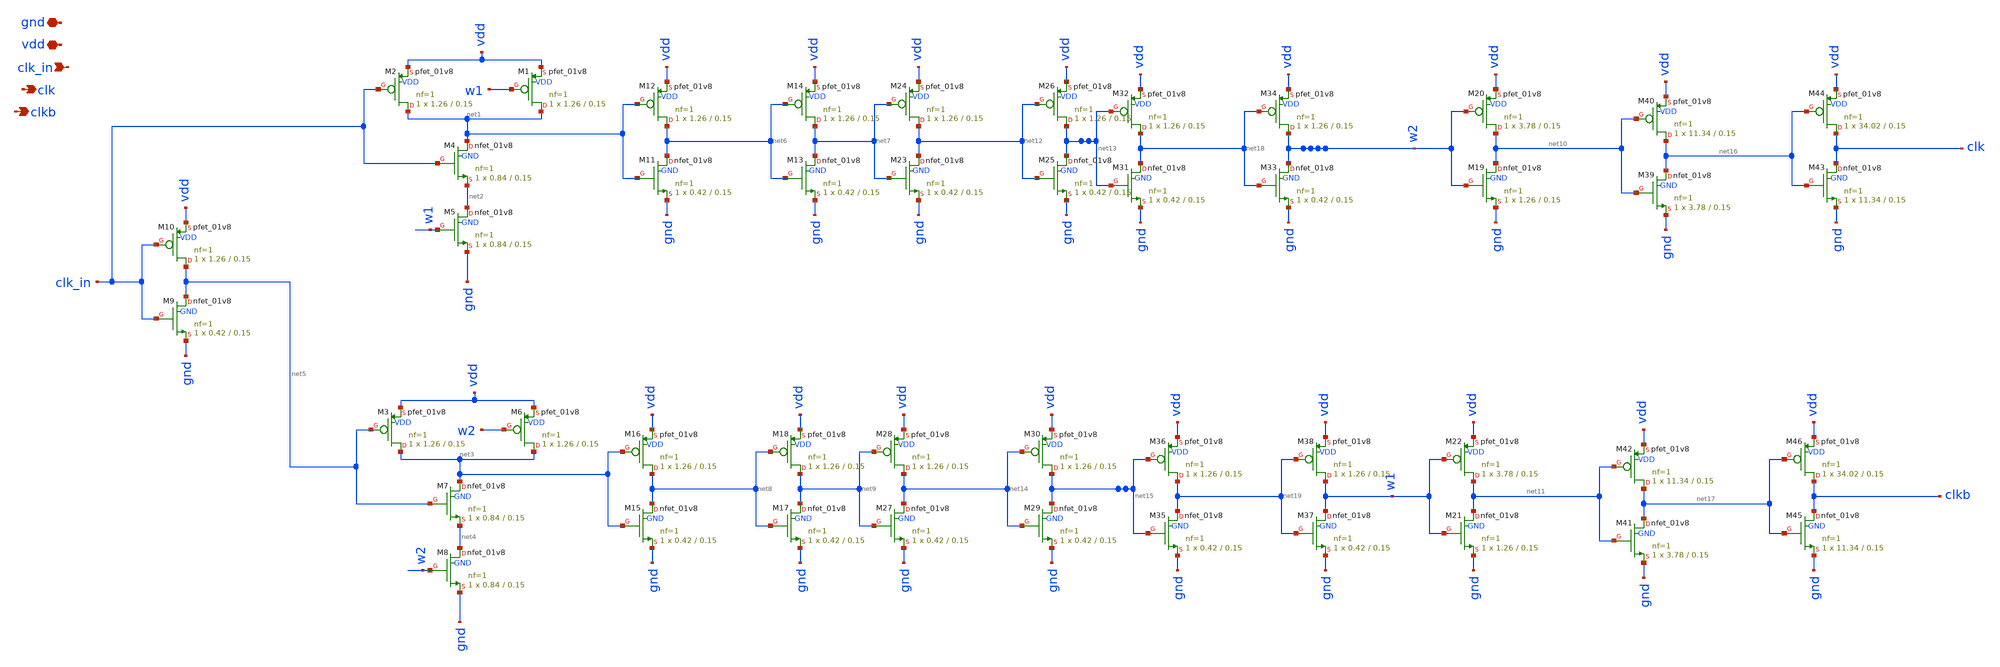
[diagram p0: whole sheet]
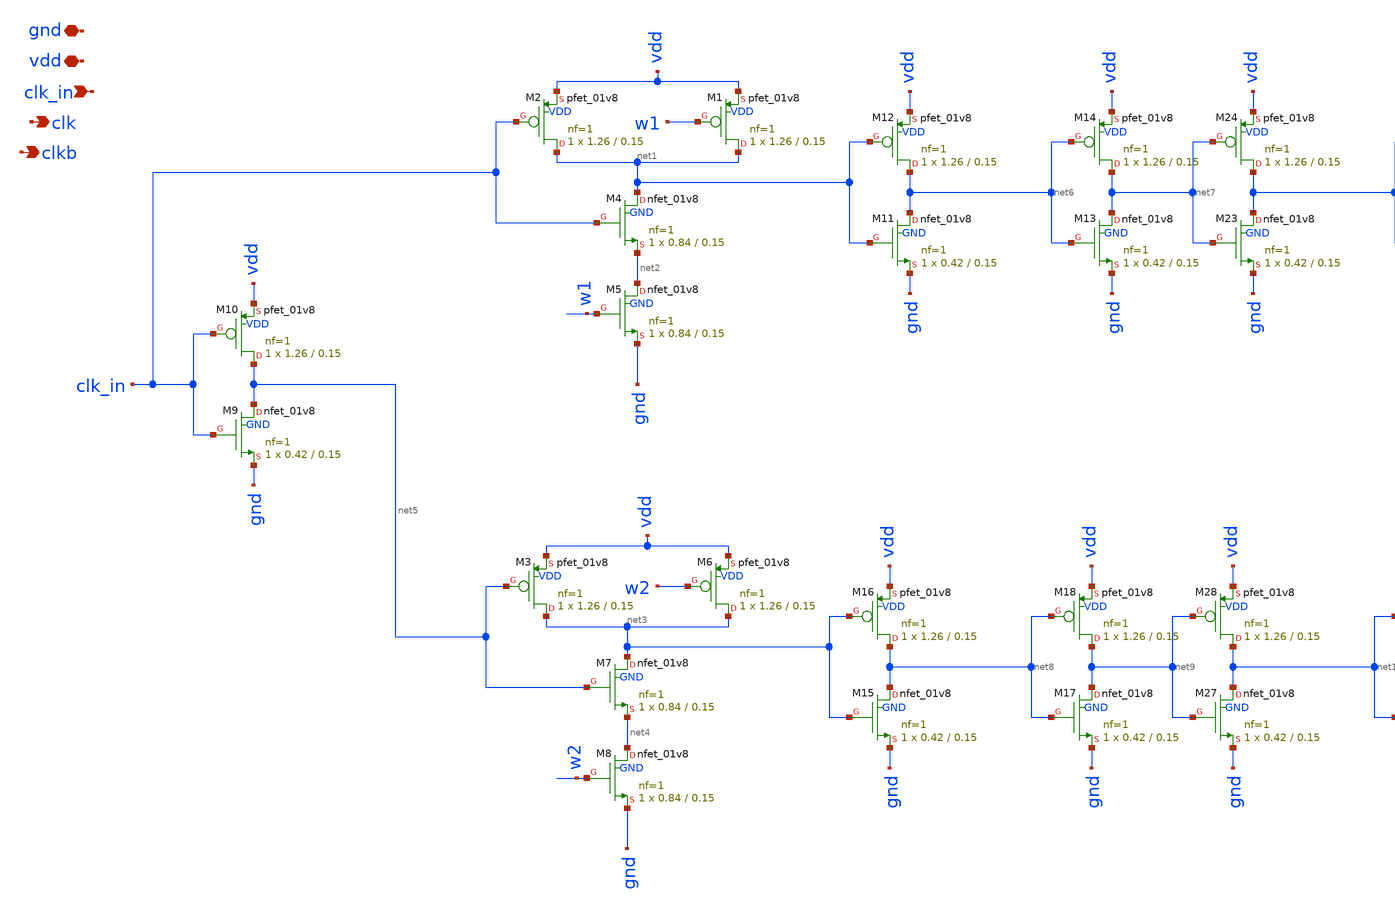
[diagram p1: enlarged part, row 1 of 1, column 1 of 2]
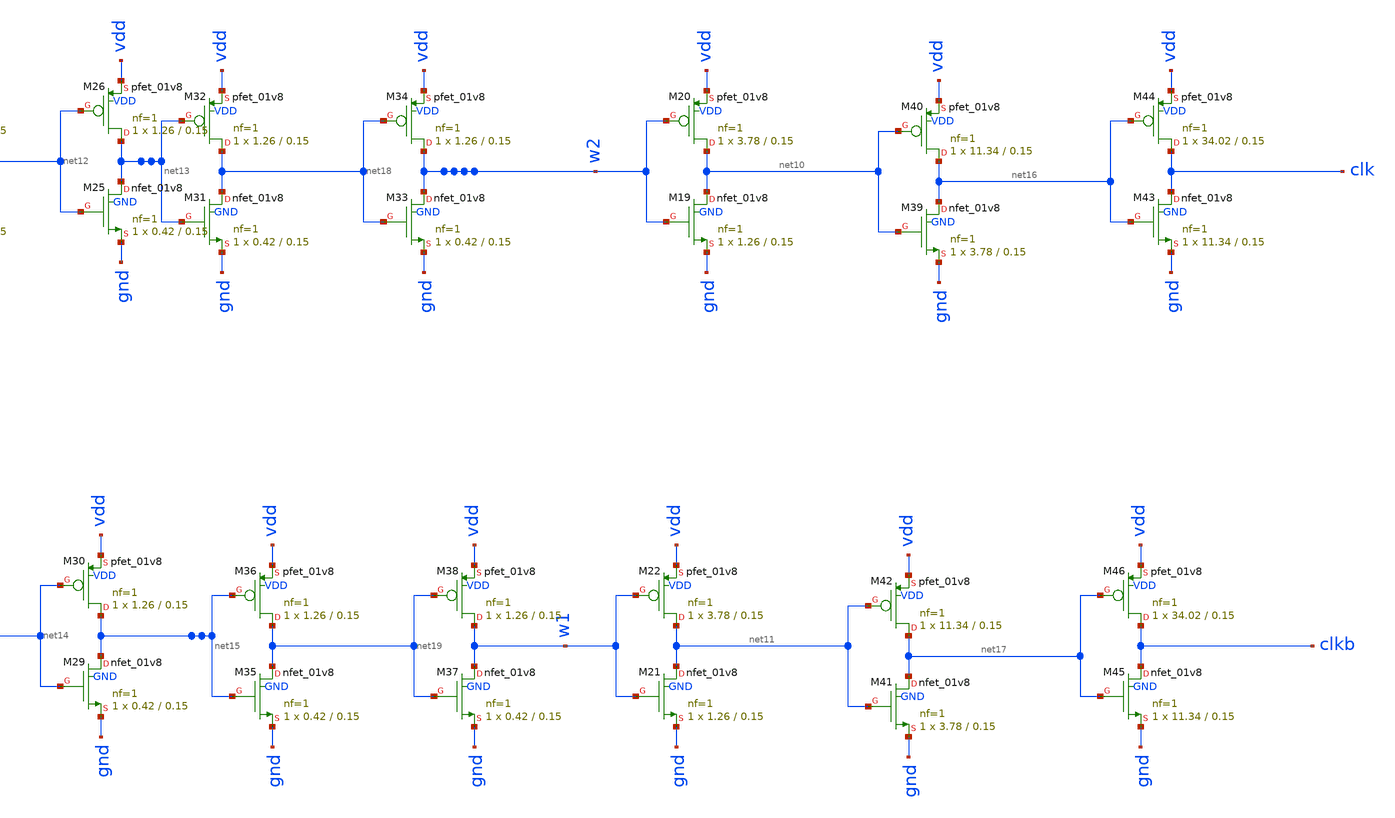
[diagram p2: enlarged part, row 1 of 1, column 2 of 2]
** sch_path: xschem/charge_pumps2/clock_1.sch
**.subckt clock_1 clk_in vdd gnd clk clkb
*.ipin clk_in
*.iopin vdd
*.iopin gnd
*.opin clk
*.opin clkb
XM2 net1 clk_in vdd VDD sky130_fd_pr__pfet_01v8 L=0.15 W=1.26 nf=1 ad='int((nf+1)/2) * W/nf * 0.29' as='int((nf+2)/2) * W/nf * 0.29'
+ pd='2*int((nf+1)/2) * (W/nf + 0.29)' ps='2*int((nf+2)/2) * (W/nf + 0.29)' nrd='0.29 / W' nrs='0.29 / W'
+ sa=0 sb=0 sd=0 mult=1 m=1
XM1 net1 w1 vdd VDD sky130_fd_pr__pfet_01v8 L=0.15 W=1.26 nf=1 ad='int((nf+1)/2) * W/nf * 0.29' as='int((nf+2)/2) * W/nf * 0.29'
+ pd='2*int((nf+1)/2) * (W/nf + 0.29)' ps='2*int((nf+2)/2) * (W/nf + 0.29)' nrd='0.29 / W' nrs='0.29 / W'
+ sa=0 sb=0 sd=0 mult=1 m=1
XM4 net1 clk_in net2 GND sky130_fd_pr__nfet_01v8 L=0.15 W=0.84 nf=1 ad='int((nf+1)/2) * W/nf * 0.29'
+ as='int((nf+2)/2) * W/nf * 0.29' pd='2*int((nf+1)/2) * (W/nf + 0.29)' ps='2*int((nf+2)/2) * (W/nf + 0.29)'
+ nrd='0.29 / W' nrs='0.29 / W' sa=0 sb=0 sd=0 mult=1 m=1
XM5 net2 w1 gnd GND sky130_fd_pr__nfet_01v8 L=0.15 W=0.84 nf=1 ad='int((nf+1)/2) * W/nf * 0.29' as='int((nf+2)/2) * W/nf * 0.29'
+ pd='2*int((nf+1)/2) * (W/nf + 0.29)' ps='2*int((nf+2)/2) * (W/nf + 0.29)' nrd='0.29 / W' nrs='0.29 / W'
+ sa=0 sb=0 sd=0 mult=1 m=1
XM3 net3 net5 vdd VDD sky130_fd_pr__pfet_01v8 L=0.15 W=1.26 nf=1 ad='int((nf+1)/2) * W/nf * 0.29' as='int((nf+2)/2) * W/nf * 0.29'
+ pd='2*int((nf+1)/2) * (W/nf + 0.29)' ps='2*int((nf+2)/2) * (W/nf + 0.29)' nrd='0.29 / W' nrs='0.29 / W'
+ sa=0 sb=0 sd=0 mult=1 m=1
XM6 net3 w2 vdd VDD sky130_fd_pr__pfet_01v8 L=0.15 W=1.26 nf=1 ad='int((nf+1)/2) * W/nf * 0.29' as='int((nf+2)/2) * W/nf * 0.29'
+ pd='2*int((nf+1)/2) * (W/nf + 0.29)' ps='2*int((nf+2)/2) * (W/nf + 0.29)' nrd='0.29 / W' nrs='0.29 / W'
+ sa=0 sb=0 sd=0 mult=1 m=1
XM7 net3 net5 net4 GND sky130_fd_pr__nfet_01v8 L=0.15 W=0.84 nf=1 ad='int((nf+1)/2) * W/nf * 0.29' as='int((nf+2)/2) * W/nf * 0.29'
+ pd='2*int((nf+1)/2) * (W/nf + 0.29)' ps='2*int((nf+2)/2) * (W/nf + 0.29)' nrd='0.29 / W' nrs='0.29 / W'
+ sa=0 sb=0 sd=0 mult=1 m=1
XM8 net4 w2 gnd GND sky130_fd_pr__nfet_01v8 L=0.15 W=0.84 nf=1 ad='int((nf+1)/2) * W/nf * 0.29' as='int((nf+2)/2) * W/nf * 0.29'
+ pd='2*int((nf+1)/2) * (W/nf + 0.29)' ps='2*int((nf+2)/2) * (W/nf + 0.29)' nrd='0.29 / W' nrs='0.29 / W'
+ sa=0 sb=0 sd=0 mult=1 m=1
XM9 net5 clk_in gnd GND sky130_fd_pr__nfet_01v8 L=0.15 W=0.42 nf=1 ad='int((nf+1)/2) * W/nf * 0.29' as='int((nf+2)/2) * W/nf * 0.29'
+ pd='2*int((nf+1)/2) * (W/nf + 0.29)' ps='2*int((nf+2)/2) * (W/nf + 0.29)' nrd='0.29 / W' nrs='0.29 / W'
+ sa=0 sb=0 sd=0 mult=1 m=1
XM10 net5 clk_in vdd VDD sky130_fd_pr__pfet_01v8 L=0.15 W=1.26 nf=1 ad='int((nf+1)/2) * W/nf * 0.29'
+ as='int((nf+2)/2) * W/nf * 0.29' pd='2*int((nf+1)/2) * (W/nf + 0.29)' ps='2*int((nf+2)/2) * (W/nf + 0.29)'
+ nrd='0.29 / W' nrs='0.29 / W' sa=0 sb=0 sd=0 mult=1 m=1
XM11 net6 net1 gnd GND sky130_fd_pr__nfet_01v8 L=0.15 W=0.42 nf=1 ad='int((nf+1)/2) * W/nf * 0.29' as='int((nf+2)/2) * W/nf * 0.29'
+ pd='2*int((nf+1)/2) * (W/nf + 0.29)' ps='2*int((nf+2)/2) * (W/nf + 0.29)' nrd='0.29 / W' nrs='0.29 / W'
+ sa=0 sb=0 sd=0 mult=1 m=1
XM12 net6 net1 vdd VDD sky130_fd_pr__pfet_01v8 L=0.15 W=1.26 nf=1 ad='int((nf+1)/2) * W/nf * 0.29' as='int((nf+2)/2) * W/nf * 0.29'
+ pd='2*int((nf+1)/2) * (W/nf + 0.29)' ps='2*int((nf+2)/2) * (W/nf + 0.29)' nrd='0.29 / W' nrs='0.29 / W'
+ sa=0 sb=0 sd=0 mult=1 m=1
XM13 net7 net6 gnd GND sky130_fd_pr__nfet_01v8 L=0.15 W=0.42 nf=1 ad='int((nf+1)/2) * W/nf * 0.29' as='int((nf+2)/2) * W/nf * 0.29'
+ pd='2*int((nf+1)/2) * (W/nf + 0.29)' ps='2*int((nf+2)/2) * (W/nf + 0.29)' nrd='0.29 / W' nrs='0.29 / W'
+ sa=0 sb=0 sd=0 mult=1 m=1
XM14 net7 net6 vdd VDD sky130_fd_pr__pfet_01v8 L=0.15 W=1.26 nf=1 ad='int((nf+1)/2) * W/nf * 0.29' as='int((nf+2)/2) * W/nf * 0.29'
+ pd='2*int((nf+1)/2) * (W/nf + 0.29)' ps='2*int((nf+2)/2) * (W/nf + 0.29)' nrd='0.29 / W' nrs='0.29 / W'
+ sa=0 sb=0 sd=0 mult=1 m=1
XM15 net8 net3 gnd GND sky130_fd_pr__nfet_01v8 L=0.15 W=0.42 nf=1 ad='int((nf+1)/2) * W/nf * 0.29' as='int((nf+2)/2) * W/nf * 0.29'
+ pd='2*int((nf+1)/2) * (W/nf + 0.29)' ps='2*int((nf+2)/2) * (W/nf + 0.29)' nrd='0.29 / W' nrs='0.29 / W'
+ sa=0 sb=0 sd=0 mult=1 m=1
XM16 net8 net3 vdd VDD sky130_fd_pr__pfet_01v8 L=0.15 W=1.26 nf=1 ad='int((nf+1)/2) * W/nf * 0.29' as='int((nf+2)/2) * W/nf * 0.29'
+ pd='2*int((nf+1)/2) * (W/nf + 0.29)' ps='2*int((nf+2)/2) * (W/nf + 0.29)' nrd='0.29 / W' nrs='0.29 / W'
+ sa=0 sb=0 sd=0 mult=1 m=1
XM17 net9 net8 gnd GND sky130_fd_pr__nfet_01v8 L=0.15 W=0.42 nf=1 ad='int((nf+1)/2) * W/nf * 0.29' as='int((nf+2)/2) * W/nf * 0.29'
+ pd='2*int((nf+1)/2) * (W/nf + 0.29)' ps='2*int((nf+2)/2) * (W/nf + 0.29)' nrd='0.29 / W' nrs='0.29 / W'
+ sa=0 sb=0 sd=0 mult=1 m=1
XM18 net9 net8 vdd VDD sky130_fd_pr__pfet_01v8 L=0.15 W=1.26 nf=1 ad='int((nf+1)/2) * W/nf * 0.29' as='int((nf+2)/2) * W/nf * 0.29'
+ pd='2*int((nf+1)/2) * (W/nf + 0.29)' ps='2*int((nf+2)/2) * (W/nf + 0.29)' nrd='0.29 / W' nrs='0.29 / W'
+ sa=0 sb=0 sd=0 mult=1 m=1
XM19 net10 w2 gnd GND sky130_fd_pr__nfet_01v8 L=0.15 W=1.26 nf=1 ad='int((nf+1)/2) * W/nf * 0.29' as='int((nf+2)/2) * W/nf * 0.29'
+ pd='2*int((nf+1)/2) * (W/nf + 0.29)' ps='2*int((nf+2)/2) * (W/nf + 0.29)' nrd='0.29 / W' nrs='0.29 / W'
+ sa=0 sb=0 sd=0 mult=1 m=1
XM20 net10 w2 vdd VDD sky130_fd_pr__pfet_01v8 L=0.15 W=3.78 nf=1 ad='int((nf+1)/2) * W/nf * 0.29' as='int((nf+2)/2) * W/nf * 0.29'
+ pd='2*int((nf+1)/2) * (W/nf + 0.29)' ps='2*int((nf+2)/2) * (W/nf + 0.29)' nrd='0.29 / W' nrs='0.29 / W'
+ sa=0 sb=0 sd=0 mult=1 m=1
XM21 net11 w1 gnd GND sky130_fd_pr__nfet_01v8 L=0.15 W=1.26 nf=1 ad='int((nf+1)/2) * W/nf * 0.29' as='int((nf+2)/2) * W/nf * 0.29'
+ pd='2*int((nf+1)/2) * (W/nf + 0.29)' ps='2*int((nf+2)/2) * (W/nf + 0.29)' nrd='0.29 / W' nrs='0.29 / W'
+ sa=0 sb=0 sd=0 mult=1 m=1
XM22 net11 w1 vdd VDD sky130_fd_pr__pfet_01v8 L=0.15 W=3.78 nf=1 ad='int((nf+1)/2) * W/nf * 0.29' as='int((nf+2)/2) * W/nf * 0.29'
+ pd='2*int((nf+1)/2) * (W/nf + 0.29)' ps='2*int((nf+2)/2) * (W/nf + 0.29)' nrd='0.29 / W' nrs='0.29 / W'
+ sa=0 sb=0 sd=0 mult=1 m=1
XM23 net12 net7 gnd GND sky130_fd_pr__nfet_01v8 L=0.15 W=0.42 nf=1 ad='int((nf+1)/2) * W/nf * 0.29' as='int((nf+2)/2) * W/nf * 0.29'
+ pd='2*int((nf+1)/2) * (W/nf + 0.29)' ps='2*int((nf+2)/2) * (W/nf + 0.29)' nrd='0.29 / W' nrs='0.29 / W'
+ sa=0 sb=0 sd=0 mult=1 m=1
XM24 net12 net7 vdd VDD sky130_fd_pr__pfet_01v8 L=0.15 W=1.26 nf=1 ad='int((nf+1)/2) * W/nf * 0.29' as='int((nf+2)/2) * W/nf * 0.29'
+ pd='2*int((nf+1)/2) * (W/nf + 0.29)' ps='2*int((nf+2)/2) * (W/nf + 0.29)' nrd='0.29 / W' nrs='0.29 / W'
+ sa=0 sb=0 sd=0 mult=1 m=1
XM25 net13 net12 gnd GND sky130_fd_pr__nfet_01v8 L=0.15 W=0.42 nf=1 ad='int((nf+1)/2) * W/nf * 0.29'
+ as='int((nf+2)/2) * W/nf * 0.29' pd='2*int((nf+1)/2) * (W/nf + 0.29)' ps='2*int((nf+2)/2) * (W/nf + 0.29)'
+ nrd='0.29 / W' nrs='0.29 / W' sa=0 sb=0 sd=0 mult=1 m=1
XM26 net13 net12 vdd VDD sky130_fd_pr__pfet_01v8 L=0.15 W=1.26 nf=1 ad='int((nf+1)/2) * W/nf * 0.29'
+ as='int((nf+2)/2) * W/nf * 0.29' pd='2*int((nf+1)/2) * (W/nf + 0.29)' ps='2*int((nf+2)/2) * (W/nf + 0.29)'
+ nrd='0.29 / W' nrs='0.29 / W' sa=0 sb=0 sd=0 mult=1 m=1
XM27 net14 net9 gnd GND sky130_fd_pr__nfet_01v8 L=0.15 W=0.42 nf=1 ad='int((nf+1)/2) * W/nf * 0.29' as='int((nf+2)/2) * W/nf * 0.29'
+ pd='2*int((nf+1)/2) * (W/nf + 0.29)' ps='2*int((nf+2)/2) * (W/nf + 0.29)' nrd='0.29 / W' nrs='0.29 / W'
+ sa=0 sb=0 sd=0 mult=1 m=1
XM28 net14 net9 vdd VDD sky130_fd_pr__pfet_01v8 L=0.15 W=1.26 nf=1 ad='int((nf+1)/2) * W/nf * 0.29' as='int((nf+2)/2) * W/nf * 0.29'
+ pd='2*int((nf+1)/2) * (W/nf + 0.29)' ps='2*int((nf+2)/2) * (W/nf + 0.29)' nrd='0.29 / W' nrs='0.29 / W'
+ sa=0 sb=0 sd=0 mult=1 m=1
XM29 net15 net14 gnd GND sky130_fd_pr__nfet_01v8 L=0.15 W=0.42 nf=1 ad='int((nf+1)/2) * W/nf * 0.29'
+ as='int((nf+2)/2) * W/nf * 0.29' pd='2*int((nf+1)/2) * (W/nf + 0.29)' ps='2*int((nf+2)/2) * (W/nf + 0.29)'
+ nrd='0.29 / W' nrs='0.29 / W' sa=0 sb=0 sd=0 mult=1 m=1
XM30 net15 net14 vdd VDD sky130_fd_pr__pfet_01v8 L=0.15 W=1.26 nf=1 ad='int((nf+1)/2) * W/nf * 0.29'
+ as='int((nf+2)/2) * W/nf * 0.29' pd='2*int((nf+1)/2) * (W/nf + 0.29)' ps='2*int((nf+2)/2) * (W/nf + 0.29)'
+ nrd='0.29 / W' nrs='0.29 / W' sa=0 sb=0 sd=0 mult=1 m=1
XM39 net16 net10 gnd GND sky130_fd_pr__nfet_01v8 L=0.15 W=3.78 nf=1 ad='int((nf+1)/2) * W/nf * 0.29'
+ as='int((nf+2)/2) * W/nf * 0.29' pd='2*int((nf+1)/2) * (W/nf + 0.29)' ps='2*int((nf+2)/2) * (W/nf + 0.29)'
+ nrd='0.29 / W' nrs='0.29 / W' sa=0 sb=0 sd=0 mult=1 m=1
XM40 net16 net10 vdd VDD sky130_fd_pr__pfet_01v8 L=0.15 W=11.34 nf=1 ad='int((nf+1)/2) * W/nf * 0.29'
+ as='int((nf+2)/2) * W/nf * 0.29' pd='2*int((nf+1)/2) * (W/nf + 0.29)' ps='2*int((nf+2)/2) * (W/nf + 0.29)'
+ nrd='0.29 / W' nrs='0.29 / W' sa=0 sb=0 sd=0 mult=1 m=1
XM41 net17 net11 gnd GND sky130_fd_pr__nfet_01v8 L=0.15 W=3.78 nf=1 ad='int((nf+1)/2) * W/nf * 0.29'
+ as='int((nf+2)/2) * W/nf * 0.29' pd='2*int((nf+1)/2) * (W/nf + 0.29)' ps='2*int((nf+2)/2) * (W/nf + 0.29)'
+ nrd='0.29 / W' nrs='0.29 / W' sa=0 sb=0 sd=0 mult=1 m=1
XM42 net17 net11 vdd VDD sky130_fd_pr__pfet_01v8 L=0.15 W=11.34 nf=1 ad='int((nf+1)/2) * W/nf * 0.29'
+ as='int((nf+2)/2) * W/nf * 0.29' pd='2*int((nf+1)/2) * (W/nf + 0.29)' ps='2*int((nf+2)/2) * (W/nf + 0.29)'
+ nrd='0.29 / W' nrs='0.29 / W' sa=0 sb=0 sd=0 mult=1 m=1
XM43 clk net16 gnd GND sky130_fd_pr__nfet_01v8 L=0.15 W=11.34 nf=1 ad='int((nf+1)/2) * W/nf * 0.29' as='int((nf+2)/2) * W/nf * 0.29'
+ pd='2*int((nf+1)/2) * (W/nf + 0.29)' ps='2*int((nf+2)/2) * (W/nf + 0.29)' nrd='0.29 / W' nrs='0.29 / W'
+ sa=0 sb=0 sd=0 mult=1 m=1
XM44 clk net16 vdd VDD sky130_fd_pr__pfet_01v8 L=0.15 W=34.02 nf=1 ad='int((nf+1)/2) * W/nf * 0.29' as='int((nf+2)/2) * W/nf * 0.29'
+ pd='2*int((nf+1)/2) * (W/nf + 0.29)' ps='2*int((nf+2)/2) * (W/nf + 0.29)' nrd='0.29 / W' nrs='0.29 / W'
+ sa=0 sb=0 sd=0 mult=1 m=1
XM45 clkb net17 gnd GND sky130_fd_pr__nfet_01v8 L=0.15 W=11.34 nf=1 ad='int((nf+1)/2) * W/nf * 0.29'
+ as='int((nf+2)/2) * W/nf * 0.29' pd='2*int((nf+1)/2) * (W/nf + 0.29)' ps='2*int((nf+2)/2) * (W/nf + 0.29)'
+ nrd='0.29 / W' nrs='0.29 / W' sa=0 sb=0 sd=0 mult=1 m=1
XM46 clkb net17 vdd VDD sky130_fd_pr__pfet_01v8 L=0.15 W=34.02 nf=1 ad='int((nf+1)/2) * W/nf * 0.29'
+ as='int((nf+2)/2) * W/nf * 0.29' pd='2*int((nf+1)/2) * (W/nf + 0.29)' ps='2*int((nf+2)/2) * (W/nf + 0.29)'
+ nrd='0.29 / W' nrs='0.29 / W' sa=0 sb=0 sd=0 mult=1 m=1
XM31 net18 net13 gnd GND sky130_fd_pr__nfet_01v8 L=0.15 W=0.42 nf=1 ad='int((nf+1)/2) * W/nf * 0.29'
+ as='int((nf+2)/2) * W/nf * 0.29' pd='2*int((nf+1)/2) * (W/nf + 0.29)' ps='2*int((nf+2)/2) * (W/nf + 0.29)'
+ nrd='0.29 / W' nrs='0.29 / W' sa=0 sb=0 sd=0 mult=1 m=1
XM32 net18 net13 vdd VDD sky130_fd_pr__pfet_01v8 L=0.15 W=1.26 nf=1 ad='int((nf+1)/2) * W/nf * 0.29'
+ as='int((nf+2)/2) * W/nf * 0.29' pd='2*int((nf+1)/2) * (W/nf + 0.29)' ps='2*int((nf+2)/2) * (W/nf + 0.29)'
+ nrd='0.29 / W' nrs='0.29 / W' sa=0 sb=0 sd=0 mult=1 m=1
XM33 w2 net18 gnd GND sky130_fd_pr__nfet_01v8 L=0.15 W=0.42 nf=1 ad='int((nf+1)/2) * W/nf * 0.29' as='int((nf+2)/2) * W/nf * 0.29'
+ pd='2*int((nf+1)/2) * (W/nf + 0.29)' ps='2*int((nf+2)/2) * (W/nf + 0.29)' nrd='0.29 / W' nrs='0.29 / W'
+ sa=0 sb=0 sd=0 mult=1 m=1
XM34 w2 net18 vdd VDD sky130_fd_pr__pfet_01v8 L=0.15 W=1.26 nf=1 ad='int((nf+1)/2) * W/nf * 0.29' as='int((nf+2)/2) * W/nf * 0.29'
+ pd='2*int((nf+1)/2) * (W/nf + 0.29)' ps='2*int((nf+2)/2) * (W/nf + 0.29)' nrd='0.29 / W' nrs='0.29 / W'
+ sa=0 sb=0 sd=0 mult=1 m=1
XM35 net19 net15 gnd GND sky130_fd_pr__nfet_01v8 L=0.15 W=0.42 nf=1 ad='int((nf+1)/2) * W/nf * 0.29'
+ as='int((nf+2)/2) * W/nf * 0.29' pd='2*int((nf+1)/2) * (W/nf + 0.29)' ps='2*int((nf+2)/2) * (W/nf + 0.29)'
+ nrd='0.29 / W' nrs='0.29 / W' sa=0 sb=0 sd=0 mult=1 m=1
XM36 net19 net15 vdd VDD sky130_fd_pr__pfet_01v8 L=0.15 W=1.26 nf=1 ad='int((nf+1)/2) * W/nf * 0.29'
+ as='int((nf+2)/2) * W/nf * 0.29' pd='2*int((nf+1)/2) * (W/nf + 0.29)' ps='2*int((nf+2)/2) * (W/nf + 0.29)'
+ nrd='0.29 / W' nrs='0.29 / W' sa=0 sb=0 sd=0 mult=1 m=1
XM37 w1 net19 gnd GND sky130_fd_pr__nfet_01v8 L=0.15 W=0.42 nf=1 ad='int((nf+1)/2) * W/nf * 0.29' as='int((nf+2)/2) * W/nf * 0.29'
+ pd='2*int((nf+1)/2) * (W/nf + 0.29)' ps='2*int((nf+2)/2) * (W/nf + 0.29)' nrd='0.29 / W' nrs='0.29 / W'
+ sa=0 sb=0 sd=0 mult=1 m=1
XM38 w1 net19 vdd VDD sky130_fd_pr__pfet_01v8 L=0.15 W=1.26 nf=1 ad='int((nf+1)/2) * W/nf * 0.29' as='int((nf+2)/2) * W/nf * 0.29'
+ pd='2*int((nf+1)/2) * (W/nf + 0.29)' ps='2*int((nf+2)/2) * (W/nf + 0.29)' nrd='0.29 / W' nrs='0.29 / W'
+ sa=0 sb=0 sd=0 mult=1 m=1
**.ends
.end
